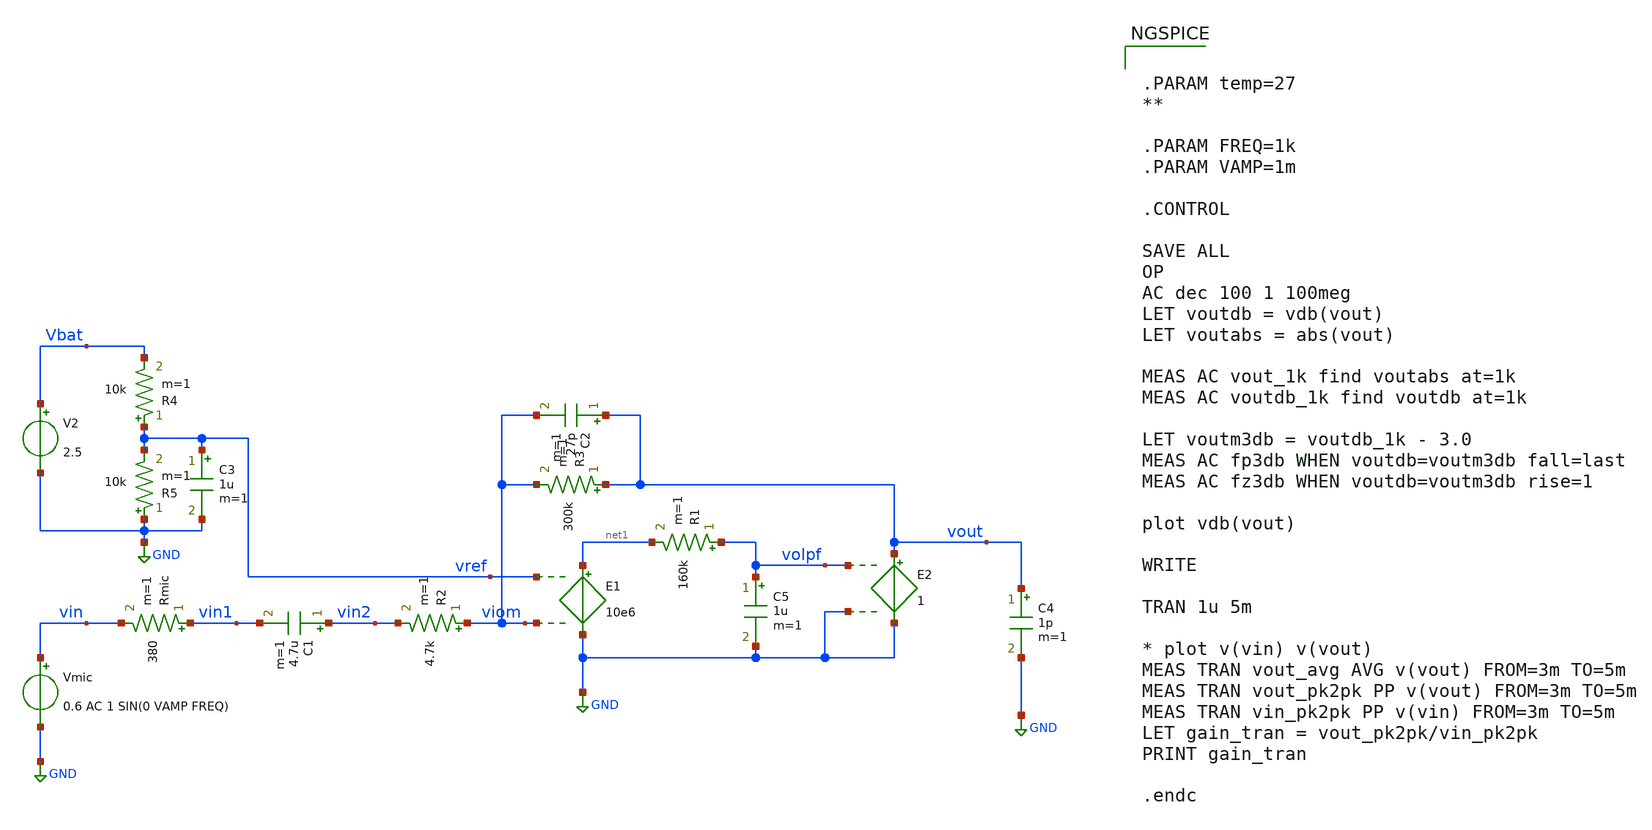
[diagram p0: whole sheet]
** sch_path: ngspice/TB_mic_amp_1pole.sch
**.subckt TB_mic_amp_1pole
Vmic vin GND 0.6 AC 1 SIN(0 VAMP FREQ)
Rmic vin1 vin 380 m=1
C1 vin2 vin1 4.7u m=1
R2 viom vin2 4.7k m=1
E1 net1 GND vref viom 10e6
V2 Vbat GND 2.5
R3 vout viom 300k m=1
C2 vout viom 27p m=1
R4 vref Vbat 10k m=1
R5 GND vref 10k m=1
C3 vref GND 1u m=1
C4 vout GND 1p m=1
R1 volpf net1 160k m=1
C5 volpf GND 1u m=1
E2 vout GND volpf GND 1
**** begin user architecture code


.PARAM temp=27
**

.PARAM FREQ=1k
.PARAM VAMP=1m

.CONTROL

SAVE ALL
OP
AC dec 100 1 100meg
LET voutdb = vdb(vout)
LET voutabs = abs(vout)

MEAS AC vout_1k find voutabs at=1k
MEAS AC voutdb_1k find voutdb at=1k

LET voutm3db = voutdb_1k - 3.0
MEAS AC fp3db WHEN voutdb=voutm3db fall=last
MEAS AC fz3db WHEN voutdb=voutm3db rise=1

plot vdb(vout)

WRITE

TRAN 1u 5m

* plot v(vin) v(vout)
MEAS TRAN vout_avg AVG v(vout) FROM=3m TO=5m
MEAS TRAN vout_pk2pk PP v(vout) FROM=3m TO=5m
MEAS TRAN vin_pk2pk PP v(vin) FROM=3m TO=5m
LET gain_tran = vout_pk2pk/vin_pk2pk
PRINT gain_tran

.endc


**** end user architecture code
**.ends
.GLOBAL GND
.end
